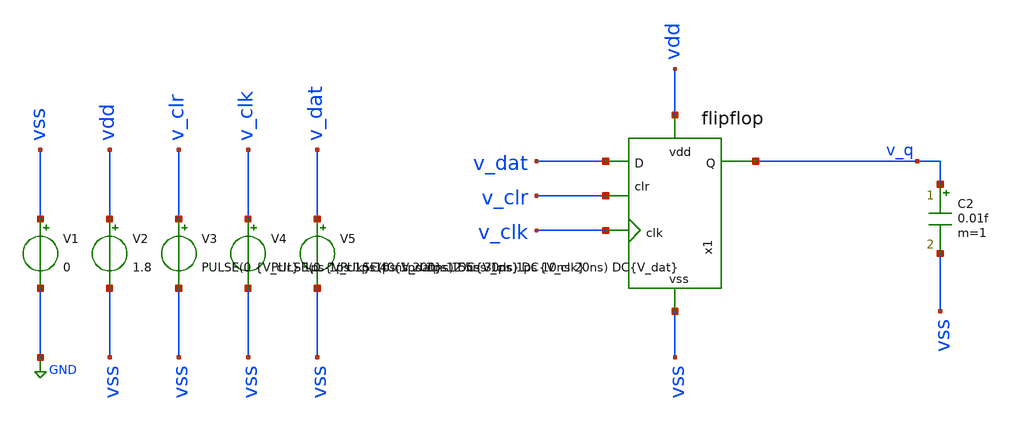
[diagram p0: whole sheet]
** sch_path: track_vlsi/martinez-sapriza/sch/tb_flipflop.sch
**.subckt tb_flipflop
V1 vss GND 0
V2 vdd vss 1.8
V3 v_clr vss PULSE(0 {V_clr} 1ps 1ps 1ps 40ns 200ns) DC{V_clr}
V4 v_clk vss PULSE(0 {V_clk} 1ps 1ps 1ps 15ns 30ns) DC{V_clk}
V5 v_dat vss PULSE(0 {V_dat} 12.5ns 1ps 1ps 10ns 20ns) DC{V_dat}
C2 v_q vss 0.01f m=1
x1 v_dat v_q v_clr v_clk vdd vss flipflop
**** begin user architecture code



* Circuit parameters
.param V_clk = 1.8
.param V_clr = 1.8
.param V_dat = 1.8
.options TEMP = 27.0

* Include
.lib /home/eamta/skywater/skywater-pdk/libraries/sky130_fd_pr_ngspice/latest/models/corners/sky130.lib TT

* Signals to save
.save all

* Simulation
.control
  tran 0.5n 200ns
  setplot tran1
  plot v(v_clr) v(v_clk) v(v_dat)
  write tb_ff_tran1.raw

  tran 0.5n 200ns
  setplot tran2
  plot v(v_q)
  write tb_ff_tran2.raw

.endc

.end



**** end user architecture code
**.ends
.GLOBAL GND
.end
